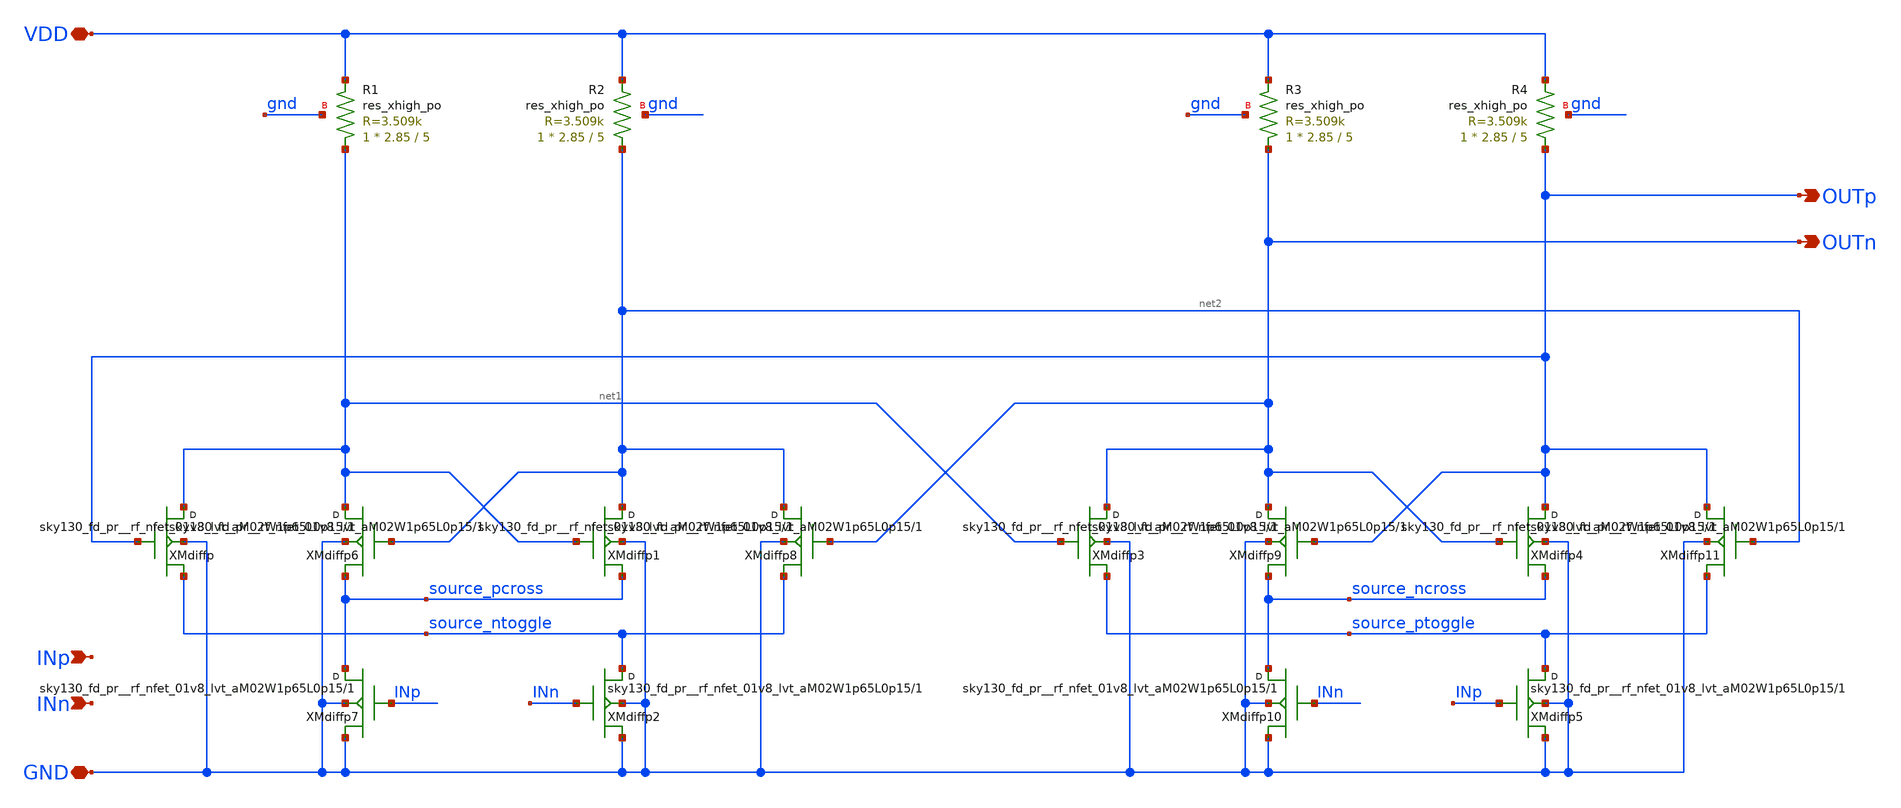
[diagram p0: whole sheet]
** sch_path: xschem/divider_cml/divider_cml.sch
**.subckt divider_cml INn OUTp VDD GND OUTn INp
*.ipin INn
*.opin OUTp
*.iopin VDD
*.iopin GND
*.opin OUTn
*.ipin INp
XXMdiffp net1 OUTp source_ntoggle GND sky130_fd_pr__rf_nfet_01v8_lvt_aM02W1p65L0p15 m=1
XXMdiffp1 net2 net1 source_pcross GND sky130_fd_pr__rf_nfet_01v8_lvt_aM02W1p65L0p15 m=1
XXMdiffp2 source_ntoggle INn GND GND sky130_fd_pr__rf_nfet_01v8_lvt_aM02W1p65L0p15 m=1
XXMdiffp3 OUTn net1 source_ptoggle GND sky130_fd_pr__rf_nfet_01v8_lvt_aM02W1p65L0p15 m=1
XXMdiffp4 OUTp OUTn source_ncross GND sky130_fd_pr__rf_nfet_01v8_lvt_aM02W1p65L0p15 m=1
XXMdiffp5 source_ptoggle INp GND GND sky130_fd_pr__rf_nfet_01v8_lvt_aM02W1p65L0p15 m=1
XXMdiffp6 net1 net2 source_pcross GND sky130_fd_pr__rf_nfet_01v8_lvt_aM02W1p65L0p15 m=1
XXMdiffp7 source_pcross INp GND GND sky130_fd_pr__rf_nfet_01v8_lvt_aM02W1p65L0p15 m=1
XXMdiffp8 net2 OUTn source_ntoggle GND sky130_fd_pr__rf_nfet_01v8_lvt_aM02W1p65L0p15 m=1
XXMdiffp9 OUTn OUTp source_ncross GND sky130_fd_pr__rf_nfet_01v8_lvt_aM02W1p65L0p15 m=1
XXMdiffp10 source_ncross INn GND GND sky130_fd_pr__rf_nfet_01v8_lvt_aM02W1p65L0p15 m=1
XXMdiffp11 OUTp net2 source_ptoggle GND sky130_fd_pr__rf_nfet_01v8_lvt_aM02W1p65L0p15 m=1
XR1 net1 VDD gnd sky130_fd_pr__res_xhigh_po W=2.85 L=5 mult=1 m=1
XR2 net2 VDD gnd sky130_fd_pr__res_xhigh_po W=2.85 L=5 mult=1 m=1
XR3 OUTn VDD gnd sky130_fd_pr__res_xhigh_po W=2.85 L=5 mult=1 m=1
XR4 OUTp VDD gnd sky130_fd_pr__res_xhigh_po W=2.85 L=5 mult=1 m=1
**.ends
.end
